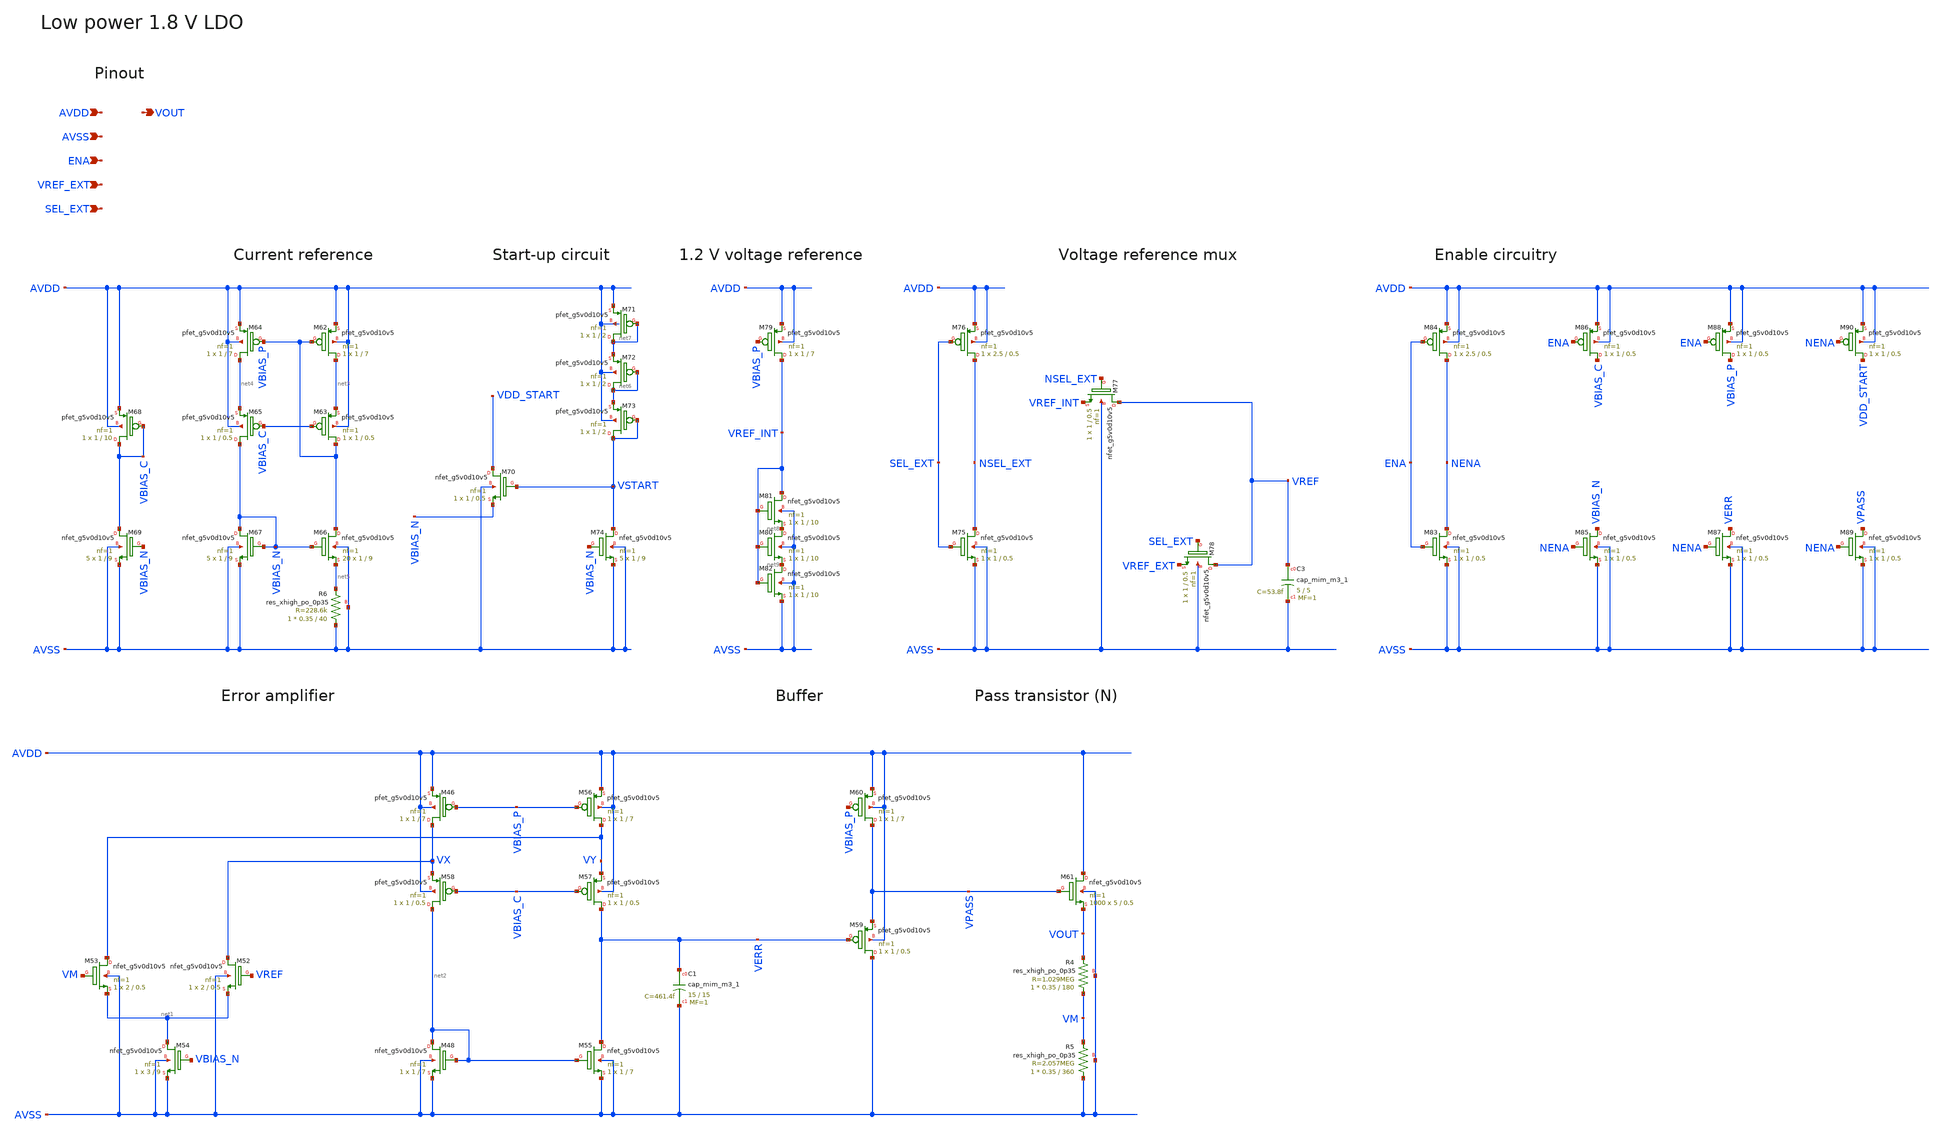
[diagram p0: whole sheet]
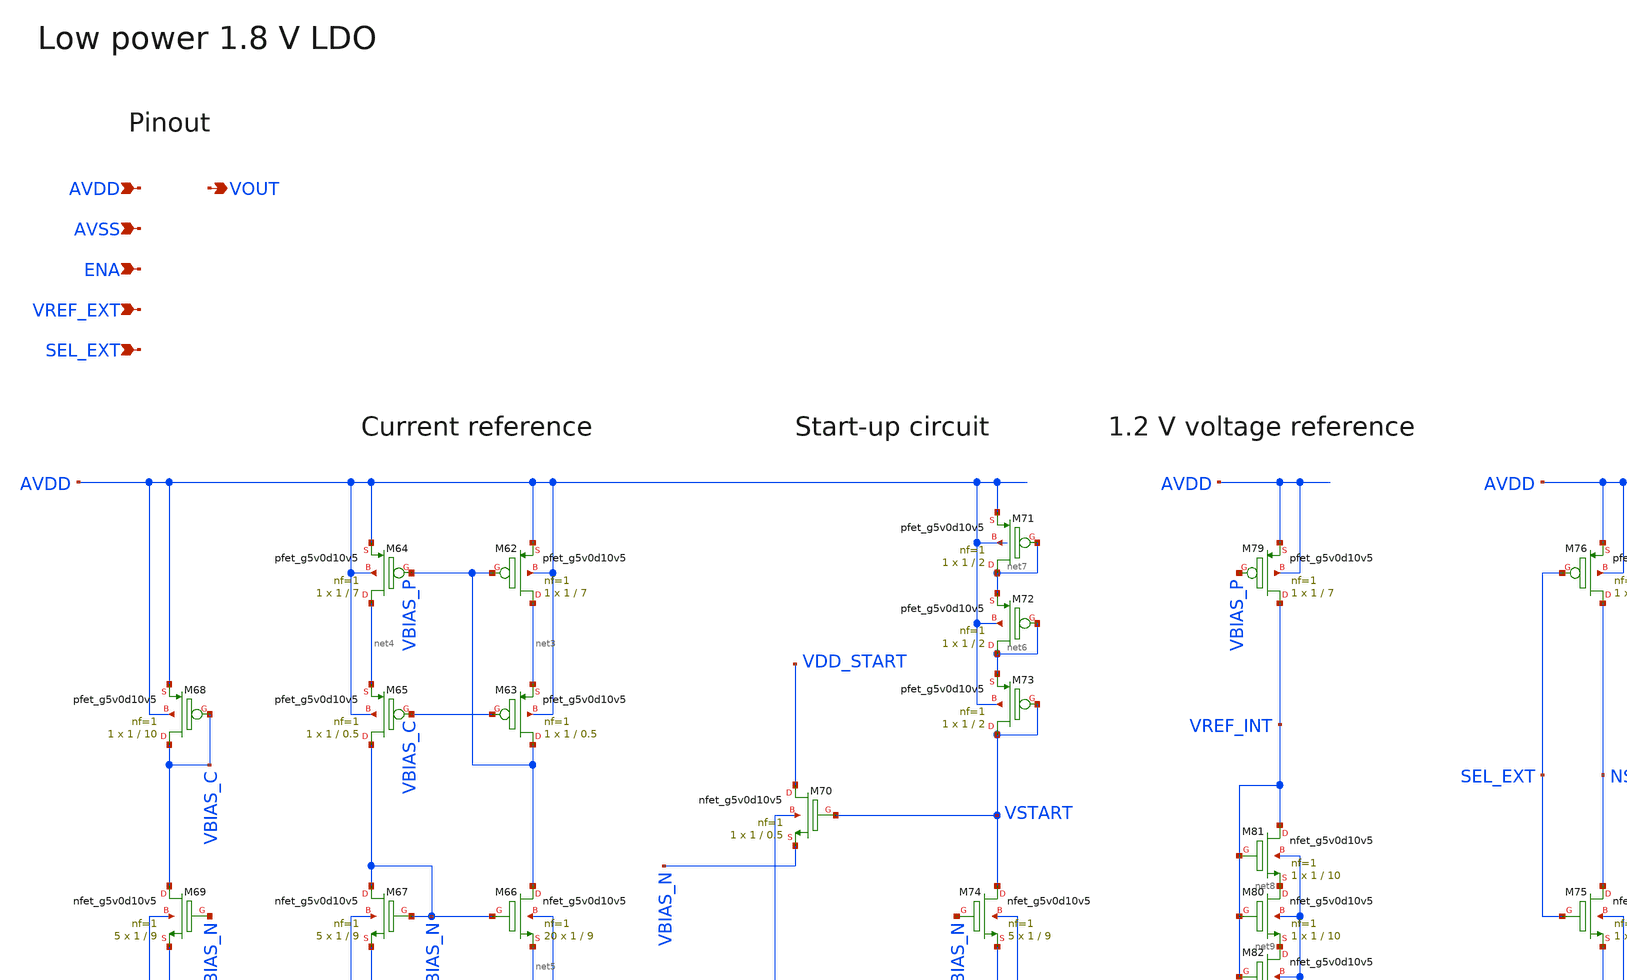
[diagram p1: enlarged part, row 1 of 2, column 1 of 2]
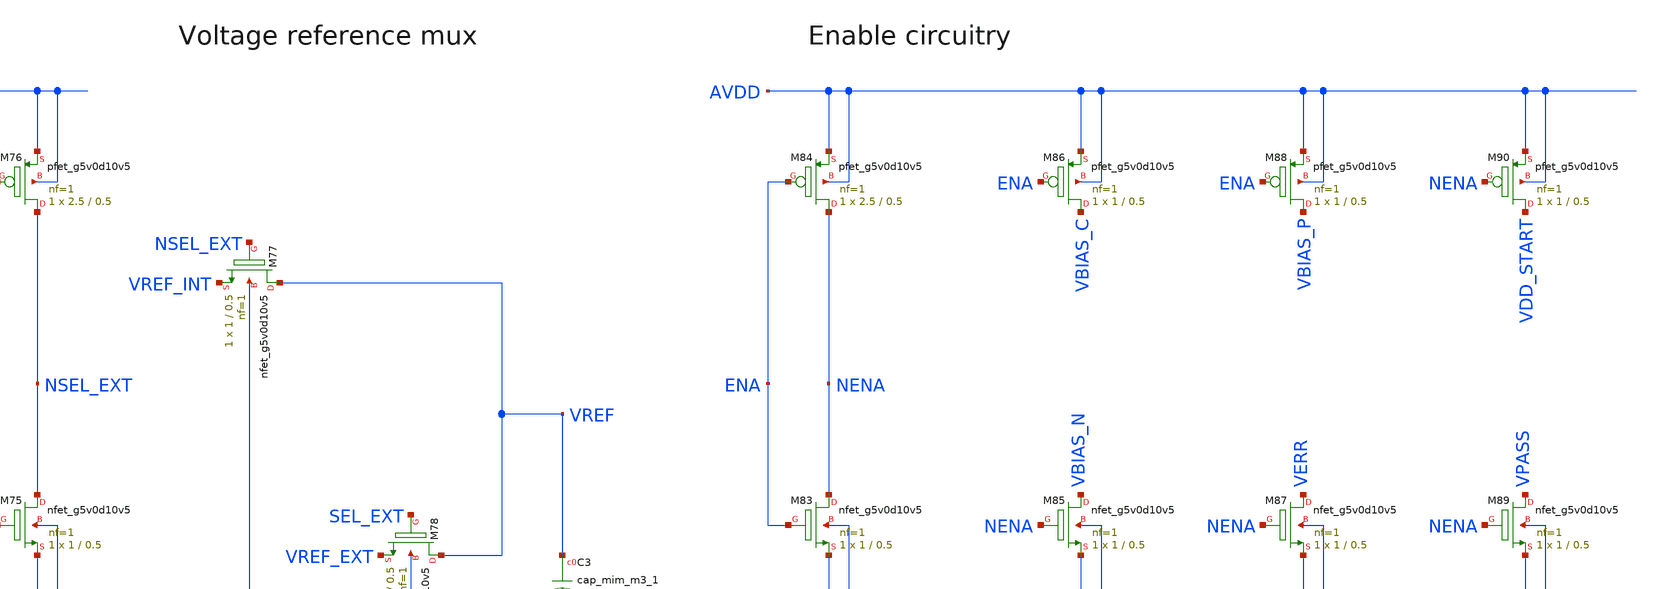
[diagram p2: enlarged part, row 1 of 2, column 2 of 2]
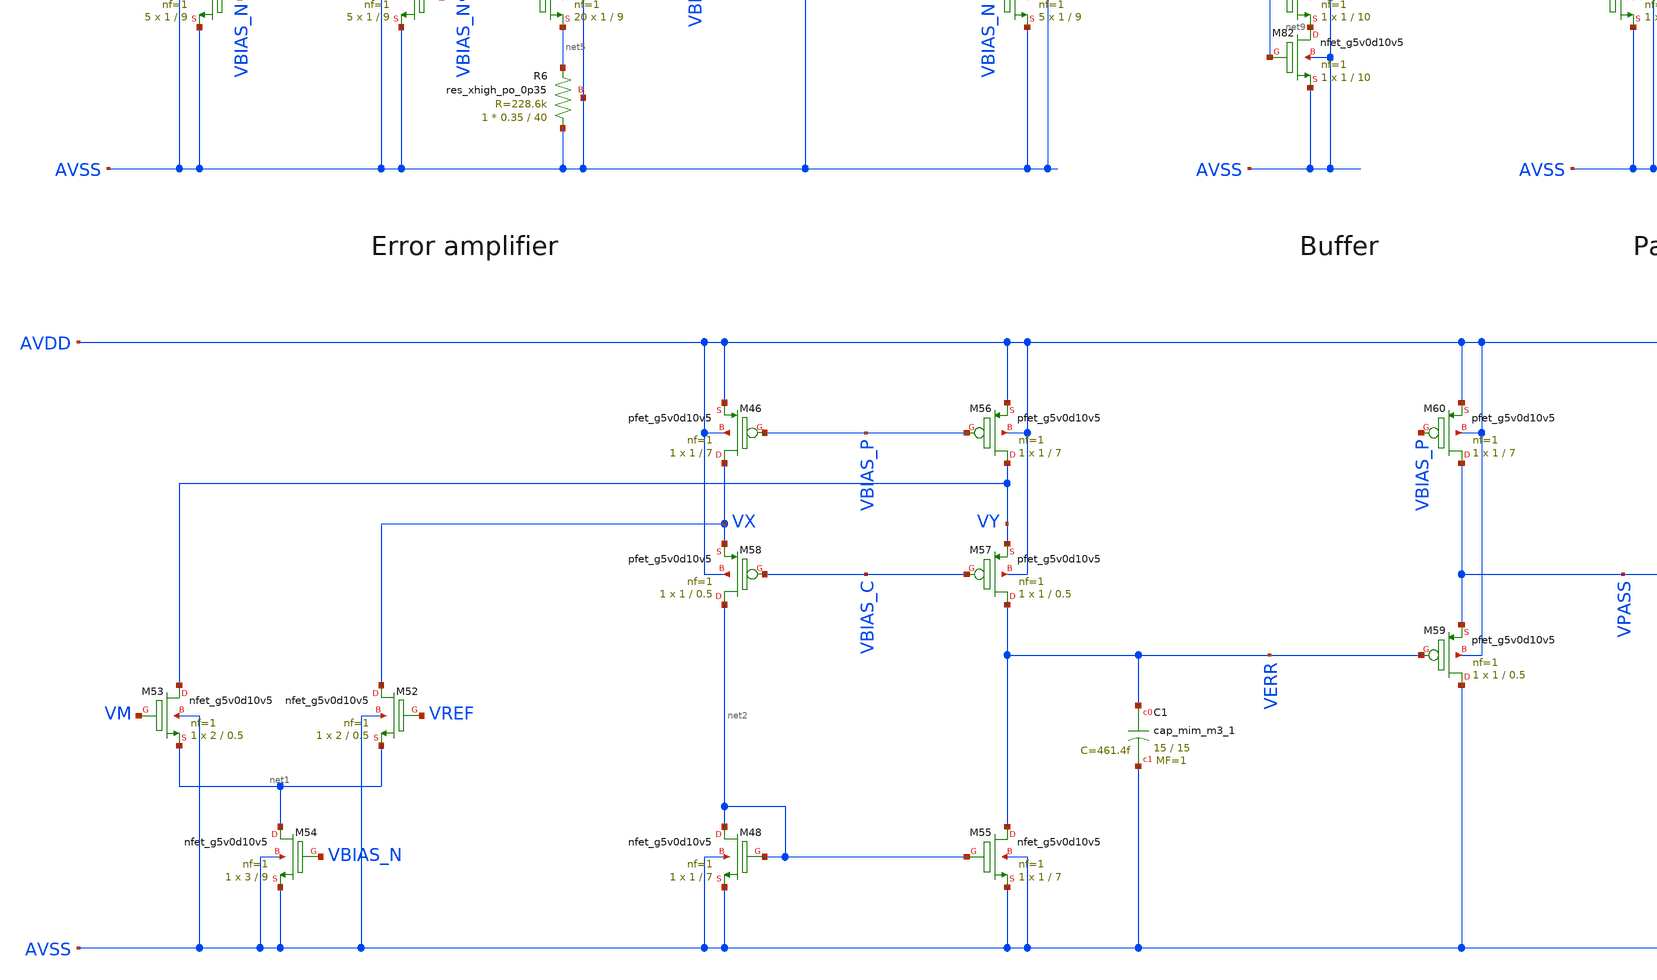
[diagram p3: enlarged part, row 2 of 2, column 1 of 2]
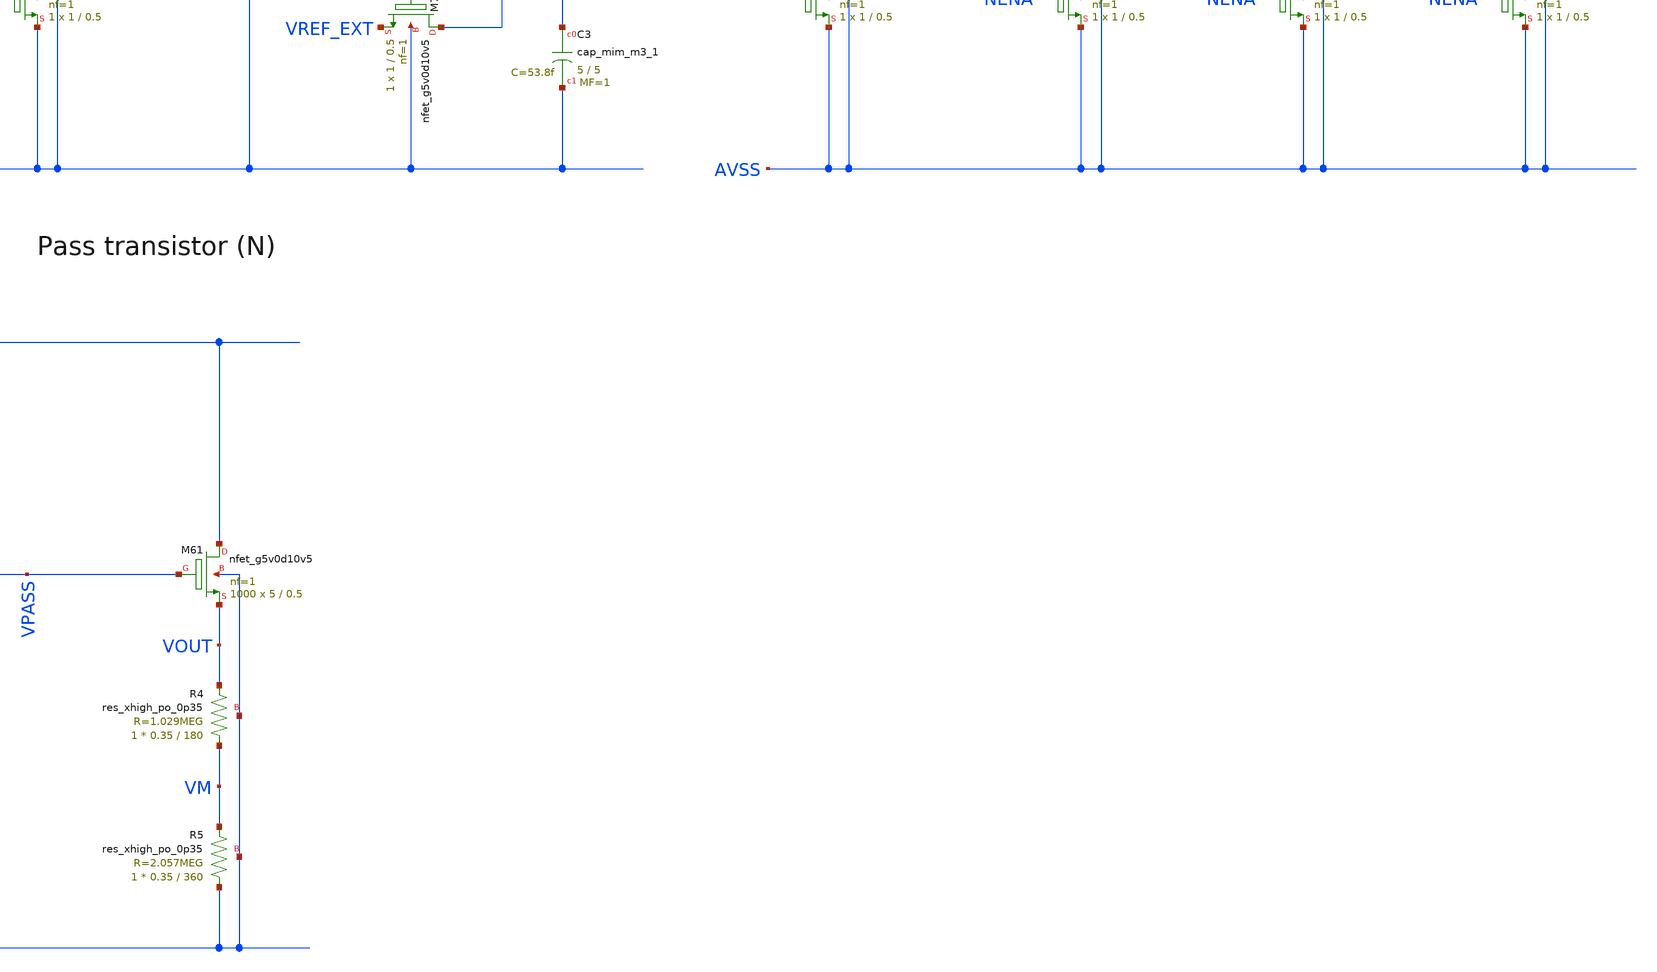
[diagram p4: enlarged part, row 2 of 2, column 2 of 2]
** sch_path: xschem/sky130_am_ip__ldo_01v8.sch
**.subckt sky130_am_ip__ldo_01v8 ENA AVDD AVSS VOUT SEL_EXT VREF_EXT
*.ipin ENA
*.ipin AVDD
*.ipin AVSS
*.opin VOUT
*.ipin SEL_EXT
*.ipin VREF_EXT
XM46 VX VBIAS_P AVDD AVDD sky130_fd_pr__pfet_g5v0d10v5 L=7 W=1 nf=1 ad='int((nf+1)/2) * W/nf * 0.29'
+ as='int((nf+2)/2) * W/nf * 0.29' pd='2*int((nf+1)/2) * (W/nf + 0.29)' ps='2*int((nf+2)/2) * (W/nf + 0.29)'
+ nrd='0.29 / W' nrs='0.29 / W' sa=0 sb=0 sd=0 mult=1 m=1
XM48 net2 net2 AVSS AVSS sky130_fd_pr__nfet_g5v0d10v5 L=7 W=1 nf=1 ad='int((nf+1)/2) * W/nf * 0.29' as='int((nf+2)/2) * W/nf * 0.29'
+ pd='2*int((nf+1)/2) * (W/nf + 0.29)' ps='2*int((nf+2)/2) * (W/nf + 0.29)' nrd='0.29 / W' nrs='0.29 / W'
+ sa=0 sb=0 sd=0 mult=1 m=1
XM52 VX VREF net1 AVSS sky130_fd_pr__nfet_g5v0d10v5 L=0.5 W=2 nf=1 ad='int((nf+1)/2) * W/nf * 0.29' as='int((nf+2)/2) * W/nf * 0.29'
+ pd='2*int((nf+1)/2) * (W/nf + 0.29)' ps='2*int((nf+2)/2) * (W/nf + 0.29)' nrd='0.29 / W' nrs='0.29 / W'
+ sa=0 sb=0 sd=0 mult=1 m=1
XM53 VY VM net1 AVSS sky130_fd_pr__nfet_g5v0d10v5 L=0.5 W=2 nf=1 ad='int((nf+1)/2) * W/nf * 0.29' as='int((nf+2)/2) * W/nf * 0.29'
+ pd='2*int((nf+1)/2) * (W/nf + 0.29)' ps='2*int((nf+2)/2) * (W/nf + 0.29)' nrd='0.29 / W' nrs='0.29 / W'
+ sa=0 sb=0 sd=0 mult=1 m=1
XM54 net1 VBIAS_N AVSS AVSS sky130_fd_pr__nfet_g5v0d10v5 L=9 W=3 nf=1 ad='int((nf+1)/2) * W/nf * 0.29'
+ as='int((nf+2)/2) * W/nf * 0.29' pd='2*int((nf+1)/2) * (W/nf + 0.29)' ps='2*int((nf+2)/2) * (W/nf + 0.29)'
+ nrd='0.29 / W' nrs='0.29 / W' sa=0 sb=0 sd=0 mult=1 m=1
XM55 VERR net2 AVSS AVSS sky130_fd_pr__nfet_g5v0d10v5 L=7 W=1 nf=1 ad='int((nf+1)/2) * W/nf * 0.29' as='int((nf+2)/2) * W/nf * 0.29'
+ pd='2*int((nf+1)/2) * (W/nf + 0.29)' ps='2*int((nf+2)/2) * (W/nf + 0.29)' nrd='0.29 / W' nrs='0.29 / W'
+ sa=0 sb=0 sd=0 mult=1 m=1
XM56 VY VBIAS_P AVDD AVDD sky130_fd_pr__pfet_g5v0d10v5 L=7 W=1 nf=1 ad='int((nf+1)/2) * W/nf * 0.29'
+ as='int((nf+2)/2) * W/nf * 0.29' pd='2*int((nf+1)/2) * (W/nf + 0.29)' ps='2*int((nf+2)/2) * (W/nf + 0.29)'
+ nrd='0.29 / W' nrs='0.29 / W' sa=0 sb=0 sd=0 mult=1 m=1
XM57 VERR VBIAS_C VY AVDD sky130_fd_pr__pfet_g5v0d10v5 L=0.5 W=1 nf=1 ad='int((nf+1)/2) * W/nf * 0.29'
+ as='int((nf+2)/2) * W/nf * 0.29' pd='2*int((nf+1)/2) * (W/nf + 0.29)' ps='2*int((nf+2)/2) * (W/nf + 0.29)'
+ nrd='0.29 / W' nrs='0.29 / W' sa=0 sb=0 sd=0 mult=1 m=1
XM58 net2 VBIAS_C VX AVDD sky130_fd_pr__pfet_g5v0d10v5 L=0.5 W=1 nf=1 ad='int((nf+1)/2) * W/nf * 0.29'
+ as='int((nf+2)/2) * W/nf * 0.29' pd='2*int((nf+1)/2) * (W/nf + 0.29)' ps='2*int((nf+2)/2) * (W/nf + 0.29)'
+ nrd='0.29 / W' nrs='0.29 / W' sa=0 sb=0 sd=0 mult=1 m=1
XM59 AVSS VERR VPASS AVDD sky130_fd_pr__pfet_g5v0d10v5 L=0.5 W=1 nf=1 ad='int((nf+1)/2) * W/nf * 0.29'
+ as='int((nf+2)/2) * W/nf * 0.29' pd='2*int((nf+1)/2) * (W/nf + 0.29)' ps='2*int((nf+2)/2) * (W/nf + 0.29)'
+ nrd='0.29 / W' nrs='0.29 / W' sa=0 sb=0 sd=0 mult=1 m=1
XM60 VPASS VBIAS_P AVDD AVDD sky130_fd_pr__pfet_g5v0d10v5 L=7 W=1 nf=1 ad='int((nf+1)/2) * W/nf * 0.29'
+ as='int((nf+2)/2) * W/nf * 0.29' pd='2*int((nf+1)/2) * (W/nf + 0.29)' ps='2*int((nf+2)/2) * (W/nf + 0.29)'
+ nrd='0.29 / W' nrs='0.29 / W' sa=0 sb=0 sd=0 mult=1 m=1
XR4 VM VOUT AVSS sky130_fd_pr__res_xhigh_po_0p35 L=180 mult=1 m=1
XR5 AVSS VM AVSS sky130_fd_pr__res_xhigh_po_0p35 L=360 mult=1 m=1
XM61 AVDD VPASS VOUT AVSS sky130_fd_pr__nfet_g5v0d10v5 L=0.5 W=5 nf=1 ad='int((nf+1)/2) * W/nf * 0.29'
+ as='int((nf+2)/2) * W/nf * 0.29' pd='2*int((nf+1)/2) * (W/nf + 0.29)' ps='2*int((nf+2)/2) * (W/nf + 0.29)'
+ nrd='0.29 / W' nrs='0.29 / W' sa=0 sb=0 sd=0 mult=1000 m=1000
XC1 VERR AVSS sky130_fd_pr__cap_mim_m3_1 W=15 L=15 MF=1 m=1
XM62 net3 VBIAS_P AVDD AVDD sky130_fd_pr__pfet_g5v0d10v5 L=7 W=1 nf=1 ad='int((nf+1)/2) * W/nf * 0.29'
+ as='int((nf+2)/2) * W/nf * 0.29' pd='2*int((nf+1)/2) * (W/nf + 0.29)' ps='2*int((nf+2)/2) * (W/nf + 0.29)'
+ nrd='0.29 / W' nrs='0.29 / W' sa=0 sb=0 sd=0 mult=1 m=1
XM63 VBIAS_P VBIAS_C net3 AVDD sky130_fd_pr__pfet_g5v0d10v5 L=0.5 W=1 nf=1 ad='int((nf+1)/2) * W/nf * 0.29'
+ as='int((nf+2)/2) * W/nf * 0.29' pd='2*int((nf+1)/2) * (W/nf + 0.29)' ps='2*int((nf+2)/2) * (W/nf + 0.29)'
+ nrd='0.29 / W' nrs='0.29 / W' sa=0 sb=0 sd=0 mult=1 m=1
XM64 net4 VBIAS_P AVDD AVDD sky130_fd_pr__pfet_g5v0d10v5 L=7 W=1 nf=1 ad='int((nf+1)/2) * W/nf * 0.29'
+ as='int((nf+2)/2) * W/nf * 0.29' pd='2*int((nf+1)/2) * (W/nf + 0.29)' ps='2*int((nf+2)/2) * (W/nf + 0.29)'
+ nrd='0.29 / W' nrs='0.29 / W' sa=0 sb=0 sd=0 mult=1 m=1
XM65 VBIAS_N VBIAS_C net4 AVDD sky130_fd_pr__pfet_g5v0d10v5 L=0.5 W=1 nf=1 ad='int((nf+1)/2) * W/nf * 0.29'
+ as='int((nf+2)/2) * W/nf * 0.29' pd='2*int((nf+1)/2) * (W/nf + 0.29)' ps='2*int((nf+2)/2) * (W/nf + 0.29)'
+ nrd='0.29 / W' nrs='0.29 / W' sa=0 sb=0 sd=0 mult=1 m=1
XM66 VBIAS_P VBIAS_N net5 AVSS sky130_fd_pr__nfet_g5v0d10v5 L=9 W=1 nf=1 ad='int((nf+1)/2) * W/nf * 0.29'
+ as='int((nf+2)/2) * W/nf * 0.29' pd='2*int((nf+1)/2) * (W/nf + 0.29)' ps='2*int((nf+2)/2) * (W/nf + 0.29)'
+ nrd='0.29 / W' nrs='0.29 / W' sa=0 sb=0 sd=0 mult=20 m=20
XM67 VBIAS_N VBIAS_N AVSS AVSS sky130_fd_pr__nfet_g5v0d10v5 L=9 W=1 nf=1 ad='int((nf+1)/2) * W/nf * 0.29'
+ as='int((nf+2)/2) * W/nf * 0.29' pd='2*int((nf+1)/2) * (W/nf + 0.29)' ps='2*int((nf+2)/2) * (W/nf + 0.29)'
+ nrd='0.29 / W' nrs='0.29 / W' sa=0 sb=0 sd=0 mult=5 m=5
XM68 VBIAS_C VBIAS_C AVDD AVDD sky130_fd_pr__pfet_g5v0d10v5 L=10 W=1 nf=1 ad='int((nf+1)/2) * W/nf * 0.29'
+ as='int((nf+2)/2) * W/nf * 0.29' pd='2*int((nf+1)/2) * (W/nf + 0.29)' ps='2*int((nf+2)/2) * (W/nf + 0.29)'
+ nrd='0.29 / W' nrs='0.29 / W' sa=0 sb=0 sd=0 mult=1 m=1
XM69 VBIAS_C VBIAS_N AVSS AVSS sky130_fd_pr__nfet_g5v0d10v5 L=9 W=1 nf=1 ad='int((nf+1)/2) * W/nf * 0.29'
+ as='int((nf+2)/2) * W/nf * 0.29' pd='2*int((nf+1)/2) * (W/nf + 0.29)' ps='2*int((nf+2)/2) * (W/nf + 0.29)'
+ nrd='0.29 / W' nrs='0.29 / W' sa=0 sb=0 sd=0 mult=5 m=5
XM70 VDD_START VSTART VBIAS_N AVSS sky130_fd_pr__nfet_g5v0d10v5 L=0.5 W=1 nf=1 ad='int((nf+1)/2) * W/nf * 0.29'
+ as='int((nf+2)/2) * W/nf * 0.29' pd='2*int((nf+1)/2) * (W/nf + 0.29)' ps='2*int((nf+2)/2) * (W/nf + 0.29)'
+ nrd='0.29 / W' nrs='0.29 / W' sa=0 sb=0 sd=0 mult=1 m=1
XM71 net7 net7 AVDD AVDD sky130_fd_pr__pfet_g5v0d10v5 L=2 W=1 nf=1 ad='int((nf+1)/2) * W/nf * 0.29' as='int((nf+2)/2) * W/nf * 0.29'
+ pd='2*int((nf+1)/2) * (W/nf + 0.29)' ps='2*int((nf+2)/2) * (W/nf + 0.29)' nrd='0.29 / W' nrs='0.29 / W'
+ sa=0 sb=0 sd=0 mult=1 m=1
XM72 net6 net6 net7 AVDD sky130_fd_pr__pfet_g5v0d10v5 L=2 W=1 nf=1 ad='int((nf+1)/2) * W/nf * 0.29' as='int((nf+2)/2) * W/nf * 0.29'
+ pd='2*int((nf+1)/2) * (W/nf + 0.29)' ps='2*int((nf+2)/2) * (W/nf + 0.29)' nrd='0.29 / W' nrs='0.29 / W'
+ sa=0 sb=0 sd=0 mult=1 m=1
XM73 VSTART VSTART net6 AVDD sky130_fd_pr__pfet_g5v0d10v5 L=2 W=1 nf=1 ad='int((nf+1)/2) * W/nf * 0.29'
+ as='int((nf+2)/2) * W/nf * 0.29' pd='2*int((nf+1)/2) * (W/nf + 0.29)' ps='2*int((nf+2)/2) * (W/nf + 0.29)'
+ nrd='0.29 / W' nrs='0.29 / W' sa=0 sb=0 sd=0 mult=1 m=1
XM74 VSTART VBIAS_N AVSS AVSS sky130_fd_pr__nfet_g5v0d10v5 L=9 W=1 nf=1 ad='int((nf+1)/2) * W/nf * 0.29'
+ as='int((nf+2)/2) * W/nf * 0.29' pd='2*int((nf+1)/2) * (W/nf + 0.29)' ps='2*int((nf+2)/2) * (W/nf + 0.29)'
+ nrd='0.29 / W' nrs='0.29 / W' sa=0 sb=0 sd=0 mult=5 m=5
XM75 NSEL_EXT SEL_EXT AVSS AVSS sky130_fd_pr__nfet_g5v0d10v5 L=0.5 W=1 nf=1 ad='int((nf+1)/2) * W/nf * 0.29'
+ as='int((nf+2)/2) * W/nf * 0.29' pd='2*int((nf+1)/2) * (W/nf + 0.29)' ps='2*int((nf+2)/2) * (W/nf + 0.29)'
+ nrd='0.29 / W' nrs='0.29 / W' sa=0 sb=0 sd=0 mult=1 m=1
XM76 NSEL_EXT SEL_EXT AVDD AVDD sky130_fd_pr__pfet_g5v0d10v5 L=0.5 W=2.5 nf=1 ad='int((nf+1)/2) * W/nf * 0.29'
+ as='int((nf+2)/2) * W/nf * 0.29' pd='2*int((nf+1)/2) * (W/nf + 0.29)' ps='2*int((nf+2)/2) * (W/nf + 0.29)'
+ nrd='0.29 / W' nrs='0.29 / W' sa=0 sb=0 sd=0 mult=1 m=1
XM77 VREF NSEL_EXT VREF_INT AVSS sky130_fd_pr__nfet_g5v0d10v5 L=0.5 W=1 nf=1 ad='int((nf+1)/2) * W/nf * 0.29'
+ as='int((nf+2)/2) * W/nf * 0.29' pd='2*int((nf+1)/2) * (W/nf + 0.29)' ps='2*int((nf+2)/2) * (W/nf + 0.29)'
+ nrd='0.29 / W' nrs='0.29 / W' sa=0 sb=0 sd=0 mult=1 m=1
XM78 VREF SEL_EXT VREF_EXT AVSS sky130_fd_pr__nfet_g5v0d10v5 L=0.5 W=1 nf=1 ad='int((nf+1)/2) * W/nf * 0.29'
+ as='int((nf+2)/2) * W/nf * 0.29' pd='2*int((nf+1)/2) * (W/nf + 0.29)' ps='2*int((nf+2)/2) * (W/nf + 0.29)'
+ nrd='0.29 / W' nrs='0.29 / W' sa=0 sb=0 sd=0 mult=1 m=1
XC3 VREF AVSS sky130_fd_pr__cap_mim_m3_1 W=5 L=5 MF=1 m=1
XR6 AVSS net5 AVSS sky130_fd_pr__res_xhigh_po_0p35 L=40 mult=1 m=1
XM79 VREF_INT VBIAS_P AVDD AVDD sky130_fd_pr__pfet_g5v0d10v5 L=7 W=1 nf=1 ad='int((nf+1)/2) * W/nf * 0.29'
+ as='int((nf+2)/2) * W/nf * 0.29' pd='2*int((nf+1)/2) * (W/nf + 0.29)' ps='2*int((nf+2)/2) * (W/nf + 0.29)'
+ nrd='0.29 / W' nrs='0.29 / W' sa=0 sb=0 sd=0 mult=1 m=1
XM80 net8 VREF_INT net9 AVSS sky130_fd_pr__nfet_g5v0d10v5 L=10 W=1 nf=1 ad='int((nf+1)/2) * W/nf * 0.29'
+ as='int((nf+2)/2) * W/nf * 0.29' pd='2*int((nf+1)/2) * (W/nf + 0.29)' ps='2*int((nf+2)/2) * (W/nf + 0.29)'
+ nrd='0.29 / W' nrs='0.29 / W' sa=0 sb=0 sd=0 mult=1 m=1
XM81 VREF_INT VREF_INT net8 AVSS sky130_fd_pr__nfet_g5v0d10v5 L=10 W=1 nf=1 ad='int((nf+1)/2) * W/nf * 0.29'
+ as='int((nf+2)/2) * W/nf * 0.29' pd='2*int((nf+1)/2) * (W/nf + 0.29)' ps='2*int((nf+2)/2) * (W/nf + 0.29)'
+ nrd='0.29 / W' nrs='0.29 / W' sa=0 sb=0 sd=0 mult=1 m=1
XM82 net9 VREF_INT AVSS AVSS sky130_fd_pr__nfet_g5v0d10v5 L=10 W=1 nf=1 ad='int((nf+1)/2) * W/nf * 0.29'
+ as='int((nf+2)/2) * W/nf * 0.29' pd='2*int((nf+1)/2) * (W/nf + 0.29)' ps='2*int((nf+2)/2) * (W/nf + 0.29)'
+ nrd='0.29 / W' nrs='0.29 / W' sa=0 sb=0 sd=0 mult=1 m=1
XM83 NENA ENA AVSS AVSS sky130_fd_pr__nfet_g5v0d10v5 L=0.5 W=1 nf=1 ad='int((nf+1)/2) * W/nf * 0.29'
+ as='int((nf+2)/2) * W/nf * 0.29' pd='2*int((nf+1)/2) * (W/nf + 0.29)' ps='2*int((nf+2)/2) * (W/nf + 0.29)'
+ nrd='0.29 / W' nrs='0.29 / W' sa=0 sb=0 sd=0 mult=1 m=1
XM84 NENA ENA AVDD AVDD sky130_fd_pr__pfet_g5v0d10v5 L=0.5 W=2.5 nf=1 ad='int((nf+1)/2) * W/nf * 0.29'
+ as='int((nf+2)/2) * W/nf * 0.29' pd='2*int((nf+1)/2) * (W/nf + 0.29)' ps='2*int((nf+2)/2) * (W/nf + 0.29)'
+ nrd='0.29 / W' nrs='0.29 / W' sa=0 sb=0 sd=0 mult=1 m=1
XM85 VBIAS_N NENA AVSS AVSS sky130_fd_pr__nfet_g5v0d10v5 L=0.5 W=1 nf=1 ad='int((nf+1)/2) * W/nf * 0.29'
+ as='int((nf+2)/2) * W/nf * 0.29' pd='2*int((nf+1)/2) * (W/nf + 0.29)' ps='2*int((nf+2)/2) * (W/nf + 0.29)'
+ nrd='0.29 / W' nrs='0.29 / W' sa=0 sb=0 sd=0 mult=1 m=1
XM86 VBIAS_C ENA AVDD AVDD sky130_fd_pr__pfet_g5v0d10v5 L=0.5 W=1 nf=1 ad='int((nf+1)/2) * W/nf * 0.29'
+ as='int((nf+2)/2) * W/nf * 0.29' pd='2*int((nf+1)/2) * (W/nf + 0.29)' ps='2*int((nf+2)/2) * (W/nf + 0.29)'
+ nrd='0.29 / W' nrs='0.29 / W' sa=0 sb=0 sd=0 mult=1 m=1
XM87 VERR NENA AVSS AVSS sky130_fd_pr__nfet_g5v0d10v5 L=0.5 W=1 nf=1 ad='int((nf+1)/2) * W/nf * 0.29'
+ as='int((nf+2)/2) * W/nf * 0.29' pd='2*int((nf+1)/2) * (W/nf + 0.29)' ps='2*int((nf+2)/2) * (W/nf + 0.29)'
+ nrd='0.29 / W' nrs='0.29 / W' sa=0 sb=0 sd=0 mult=1 m=1
XM88 VBIAS_P ENA AVDD AVDD sky130_fd_pr__pfet_g5v0d10v5 L=0.5 W=1 nf=1 ad='int((nf+1)/2) * W/nf * 0.29'
+ as='int((nf+2)/2) * W/nf * 0.29' pd='2*int((nf+1)/2) * (W/nf + 0.29)' ps='2*int((nf+2)/2) * (W/nf + 0.29)'
+ nrd='0.29 / W' nrs='0.29 / W' sa=0 sb=0 sd=0 mult=1 m=1
XM89 VPASS NENA AVSS AVSS sky130_fd_pr__nfet_g5v0d10v5 L=0.5 W=1 nf=1 ad='int((nf+1)/2) * W/nf * 0.29'
+ as='int((nf+2)/2) * W/nf * 0.29' pd='2*int((nf+1)/2) * (W/nf + 0.29)' ps='2*int((nf+2)/2) * (W/nf + 0.29)'
+ nrd='0.29 / W' nrs='0.29 / W' sa=0 sb=0 sd=0 mult=1 m=1
XM90 VDD_START NENA AVDD AVDD sky130_fd_pr__pfet_g5v0d10v5 L=0.5 W=1 nf=1 ad='int((nf+1)/2) * W/nf * 0.29'
+ as='int((nf+2)/2) * W/nf * 0.29' pd='2*int((nf+1)/2) * (W/nf + 0.29)' ps='2*int((nf+2)/2) * (W/nf + 0.29)'
+ nrd='0.29 / W' nrs='0.29 / W' sa=0 sb=0 sd=0 mult=1 m=1
**.ends
.end
